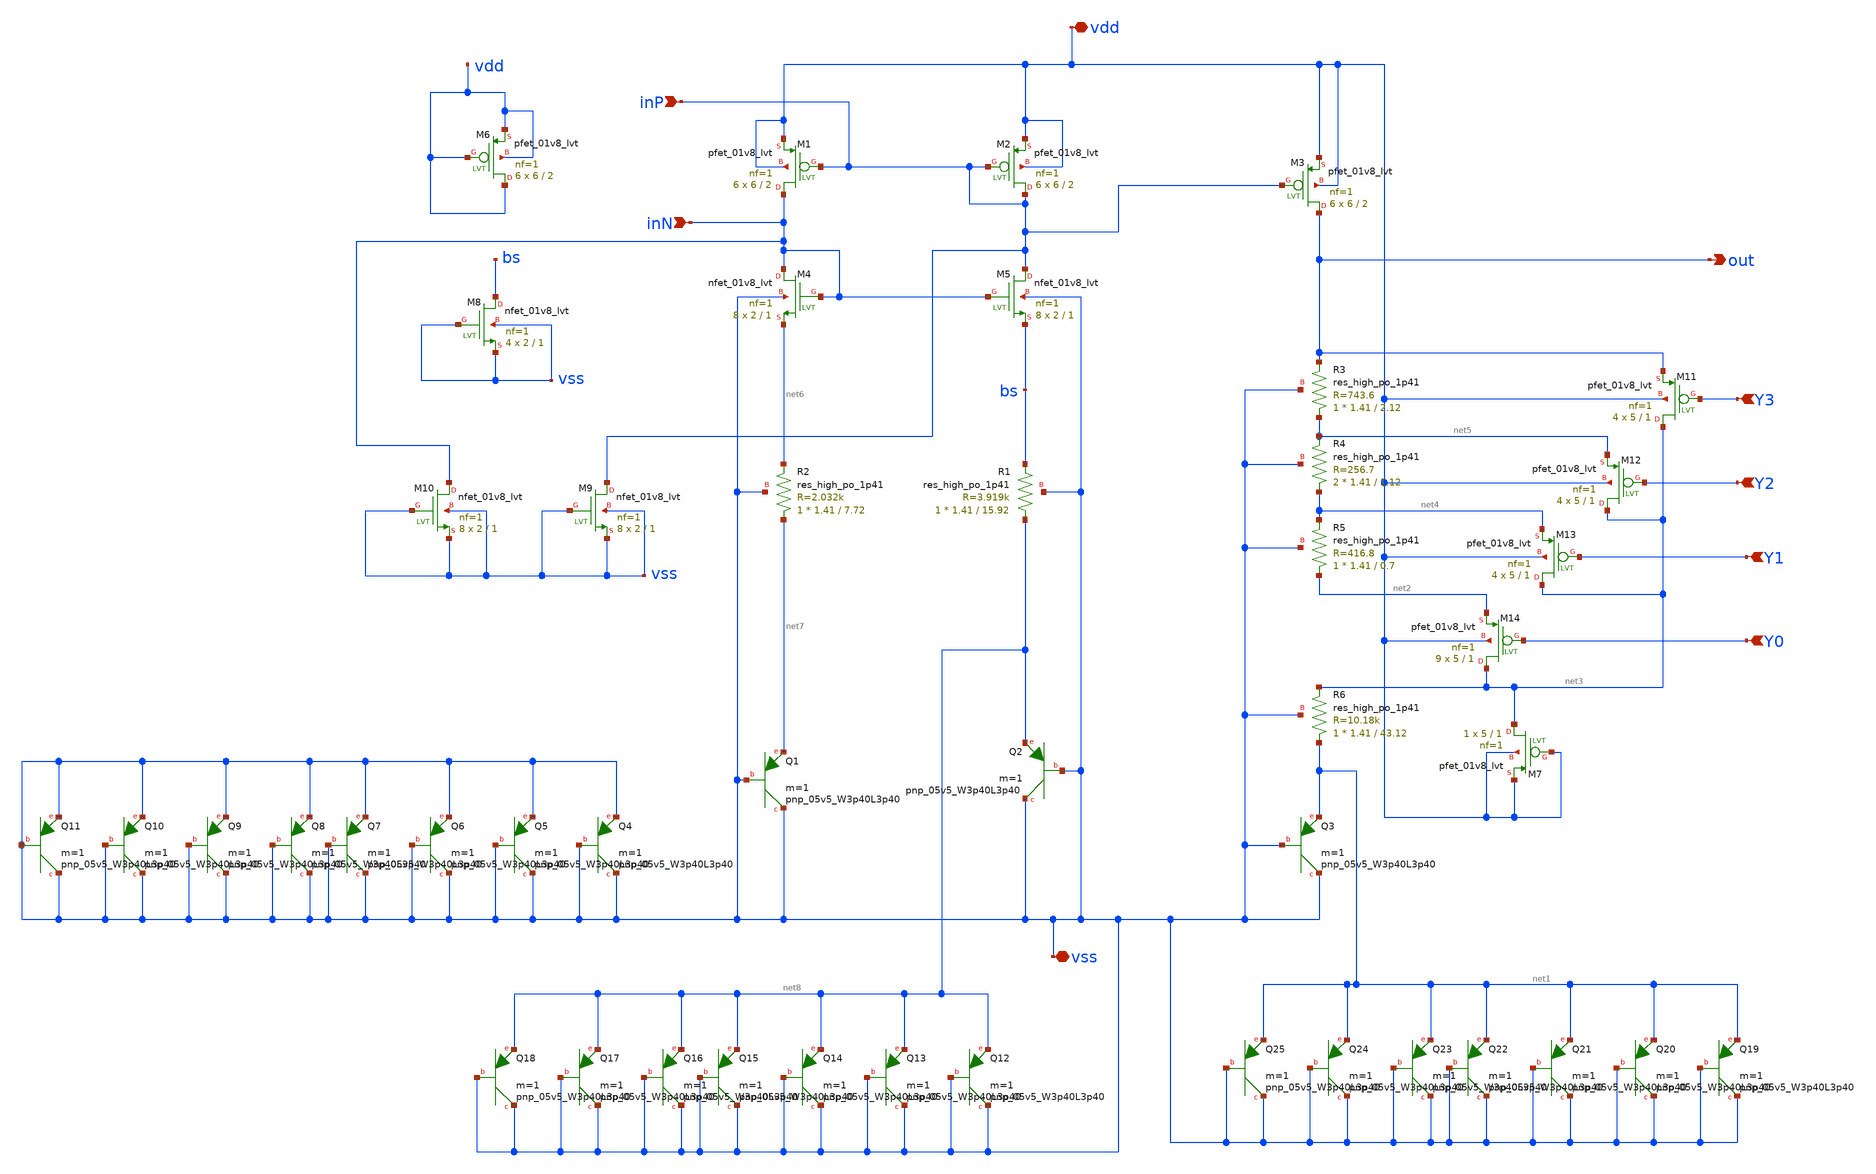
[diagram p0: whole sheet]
** sch_path: BGR_TOP_SKY130A/BGR_coreAndVrefBranch.sch
**.subckt BGR_coreAndVrefBranch Y3 Y2 Y1 Y0 vdd vss inP inN out
*.ipin Y3
*.ipin Y2
*.ipin Y1
*.ipin Y0
*.iopin vdd
*.iopin vss
*.ipin inP
*.ipin inN
*.opin out
XM11 net3 Y3 out vdd sky130_fd_pr__pfet_01v8_lvt L=1 W=5 nf=1 ad='int((1 + 1)/2) * 5 / 1 * 0.29' as='int((1 + 2)/2) * 5 / 1 * 0.29'
+ pd='2*int((1 + 1)/2) * (5 / 1 + 0.29)' ps='2*int((1 + 2)/2) * (5 / 1 + 0.29)' nrd='0.29 / 5 ' nrs='0.29 / 5 '
+ sa=0 sb=0 sd=0 mult=4 m=4
XM12 net3 Y2 net5 vdd sky130_fd_pr__pfet_01v8_lvt L=1 W=5 nf=1 ad='int((1 + 1)/2) * 5 / 1 * 0.29' as='int((1 + 2)/2) * 5 / 1 * 0.29'
+ pd='2*int((1 + 1)/2) * (5 / 1 + 0.29)' ps='2*int((1 + 2)/2) * (5 / 1 + 0.29)' nrd='0.29 / 5 ' nrs='0.29 / 5 '
+ sa=0 sb=0 sd=0 mult=4 m=4
XM13 net3 Y1 net4 vdd sky130_fd_pr__pfet_01v8_lvt L=1 W=5 nf=1 ad='int((1 + 1)/2) * 5 / 1 * 0.29' as='int((1 + 2)/2) * 5 / 1 * 0.29'
+ pd='2*int((1 + 1)/2) * (5 / 1 + 0.29)' ps='2*int((1 + 2)/2) * (5 / 1 + 0.29)' nrd='0.29 / 5 ' nrs='0.29 / 5 '
+ sa=0 sb=0 sd=0 mult=4 m=4
XM14 net3 Y0 net2 vdd sky130_fd_pr__pfet_01v8_lvt L=1 W=5 nf=1 ad='int((1 + 1)/2) * 5 / 1 * 0.29' as='int((1 + 2)/2) * 5 / 1 * 0.29'
+ pd='2*int((1 + 1)/2) * (5 / 1 + 0.29)' ps='2*int((1 + 2)/2) * (5 / 1 + 0.29)' nrd='0.29 / 5 ' nrs='0.29 / 5 '
+ sa=0 sb=0 sd=0 mult=9 m=9
XR3 net5 out vss sky130_fd_pr__res_high_po_1p41 L=2.12 mult=1 m=1
XR4 net4 net5 vss sky130_fd_pr__res_high_po_1p41 L=1.12 mult=2 m=2
XR5 net2 net4 vss sky130_fd_pr__res_high_po_1p41 L=0.7 mult=1 m=1
XR6 net1 net3 vss sky130_fd_pr__res_high_po_1p41 L=43.12 mult=1 m=1
XM1 inN inP vdd vdd sky130_fd_pr__pfet_01v8_lvt L=2 W=6 nf=1 ad='int((1 + 1)/2) * 6 / 1 * 0.29' as='int((1 + 2)/2) * 6 / 1 * 0.29'
+ pd='2*int((1 + 1)/2) * (6 / 1 + 0.29)' ps='2*int((1 + 2)/2) * (6 / 1 + 0.29)' nrd='0.29 / 6 ' nrs='0.29 / 6 '
+ sa=0 sb=0 sd=0 mult=6 m=6
XM2 inP inP vdd vdd sky130_fd_pr__pfet_01v8_lvt L=2 W=6 nf=1 ad='int((1 + 1)/2) * 6 / 1 * 0.29' as='int((1 + 2)/2) * 6 / 1 * 0.29'
+ pd='2*int((1 + 1)/2) * (6 / 1 + 0.29)' ps='2*int((1 + 2)/2) * (6 / 1 + 0.29)' nrd='0.29 / 6 ' nrs='0.29 / 6 '
+ sa=0 sb=0 sd=0 mult=6 m=6
XM3 out inP vdd vdd sky130_fd_pr__pfet_01v8_lvt L=2 W=6 nf=1 ad='int((1 + 1)/2) * 6 / 1 * 0.29' as='int((1 + 2)/2) * 6 / 1 * 0.29'
+ pd='2*int((1 + 1)/2) * (6 / 1 + 0.29)' ps='2*int((1 + 2)/2) * (6 / 1 + 0.29)' nrd='0.29 / 6 ' nrs='0.29 / 6 '
+ sa=0 sb=0 sd=0 mult=6 m=6
XM4 inN inN net6 vss sky130_fd_pr__nfet_01v8_lvt L=1 W=2 nf=1 ad='int((1 + 1)/2) * 2 / 1 * 0.29' as='int((1 + 2)/2) * 2 / 1 * 0.29'
+ pd='2*int((1 + 1)/2) * (2 / 1 + 0.29)' ps='2*int((1 + 2)/2) * (2 / 1 + 0.29)' nrd='0.29 / 2 ' nrs='0.29 / 2 '
+ sa=0 sb=0 sd=0 mult=8 m=8
XM5 inP inN bs vss sky130_fd_pr__nfet_01v8_lvt L=1 W=2 nf=1 ad='int((1 + 1)/2) * 2 / 1 * 0.29' as='int((1 + 2)/2) * 2 / 1 * 0.29'
+ pd='2*int((1 + 1)/2) * (2 / 1 + 0.29)' ps='2*int((1 + 2)/2) * (2 / 1 + 0.29)' nrd='0.29 / 2 ' nrs='0.29 / 2 '
+ sa=0 sb=0 sd=0 mult=8 m=8
XR1 net8 bs vss sky130_fd_pr__res_high_po_1p41 L=15.92 mult=1 m=1
XR2 net7 net6 vss sky130_fd_pr__res_high_po_1p41 L=7.72 mult=1 m=1
XQ1 vss vss net7 sky130_fd_pr__pnp_05v5_W3p40L3p40 m=1
XQ2 vss vss net8 sky130_fd_pr__pnp_05v5_W3p40L3p40 m=1
XQ3 vss vss net1 sky130_fd_pr__pnp_05v5_W3p40L3p40 m=1
XM6 vdd vdd vdd vdd sky130_fd_pr__pfet_01v8_lvt L=2 W=6 nf=1 ad='int((1 + 1)/2) * 6 / 1 * 0.29' as='int((1 + 2)/2) * 6 / 1 * 0.29'
+ pd='2*int((1 + 1)/2) * (6 / 1 + 0.29)' ps='2*int((1 + 2)/2) * (6 / 1 + 0.29)' nrd='0.29 / 6 ' nrs='0.29 / 6 '
+ sa=0 sb=0 sd=0 mult=6 m=6
XM7 net3 vdd vdd vdd sky130_fd_pr__pfet_01v8_lvt L=1 W=5 nf=1 ad='int((1 + 1)/2) * 5 / 1 * 0.29' as='int((1 + 2)/2) * 5 / 1 * 0.29'
+ pd='2*int((1 + 1)/2) * (5 / 1 + 0.29)' ps='2*int((1 + 2)/2) * (5 / 1 + 0.29)' nrd='0.29 / 5 ' nrs='0.29 / 5 '
+ sa=0 sb=0 sd=0 mult=1 m=1
XM8 bs vss vss vss sky130_fd_pr__nfet_01v8_lvt L=1 W=2 nf=1 ad='int((1 + 1)/2) * 2 / 1 * 0.29' as='int((1 + 2)/2) * 2 / 1 * 0.29'
+ pd='2*int((1 + 1)/2) * (2 / 1 + 0.29)' ps='2*int((1 + 2)/2) * (2 / 1 + 0.29)' nrd='0.29 / 2 ' nrs='0.29 / 2 '
+ sa=0 sb=0 sd=0 mult=4 m=4
XM9 inP vss vss vss sky130_fd_pr__nfet_01v8_lvt L=1 W=2 nf=1 ad='int((1 + 1)/2) * 2 / 1 * 0.29' as='int((1 + 2)/2) * 2 / 1 * 0.29'
+ pd='2*int((1 + 1)/2) * (2 / 1 + 0.29)' ps='2*int((1 + 2)/2) * (2 / 1 + 0.29)' nrd='0.29 / 2 ' nrs='0.29 / 2 '
+ sa=0 sb=0 sd=0 mult=8 m=8
XM10 inN vss vss vss sky130_fd_pr__nfet_01v8_lvt L=1 W=2 nf=1 ad='int((1 + 1)/2) * 2 / 1 * 0.29' as='int((1 + 2)/2) * 2 / 1 * 0.29'
+ pd='2*int((1 + 1)/2) * (2 / 1 + 0.29)' ps='2*int((1 + 2)/2) * (2 / 1 + 0.29)' nrd='0.29 / 2 ' nrs='0.29 / 2 '
+ sa=0 sb=0 sd=0 mult=8 m=8
XQ4 vss vss vss sky130_fd_pr__pnp_05v5_W3p40L3p40 m=1
XQ5 vss vss vss sky130_fd_pr__pnp_05v5_W3p40L3p40 m=1
XQ6 vss vss vss sky130_fd_pr__pnp_05v5_W3p40L3p40 m=1
XQ7 vss vss vss sky130_fd_pr__pnp_05v5_W3p40L3p40 m=1
XQ8 vss vss vss sky130_fd_pr__pnp_05v5_W3p40L3p40 m=1
XQ9 vss vss vss sky130_fd_pr__pnp_05v5_W3p40L3p40 m=1
XQ10 vss vss vss sky130_fd_pr__pnp_05v5_W3p40L3p40 m=1
XQ11 vss vss vss sky130_fd_pr__pnp_05v5_W3p40L3p40 m=1
XQ12 vss vss net8 sky130_fd_pr__pnp_05v5_W3p40L3p40 m=1
XQ13 vss vss net8 sky130_fd_pr__pnp_05v5_W3p40L3p40 m=1
XQ14 vss vss net8 sky130_fd_pr__pnp_05v5_W3p40L3p40 m=1
XQ15 vss vss net8 sky130_fd_pr__pnp_05v5_W3p40L3p40 m=1
XQ16 vss vss net8 sky130_fd_pr__pnp_05v5_W3p40L3p40 m=1
XQ17 vss vss net8 sky130_fd_pr__pnp_05v5_W3p40L3p40 m=1
XQ18 vss vss net8 sky130_fd_pr__pnp_05v5_W3p40L3p40 m=1
XQ19 vss vss net1 sky130_fd_pr__pnp_05v5_W3p40L3p40 m=1
XQ20 vss vss net1 sky130_fd_pr__pnp_05v5_W3p40L3p40 m=1
XQ21 vss vss net1 sky130_fd_pr__pnp_05v5_W3p40L3p40 m=1
XQ22 vss vss net1 sky130_fd_pr__pnp_05v5_W3p40L3p40 m=1
XQ23 vss vss net1 sky130_fd_pr__pnp_05v5_W3p40L3p40 m=1
XQ24 vss vss net1 sky130_fd_pr__pnp_05v5_W3p40L3p40 m=1
XQ25 vss vss net1 sky130_fd_pr__pnp_05v5_W3p40L3p40 m=1
**.ends
.end
